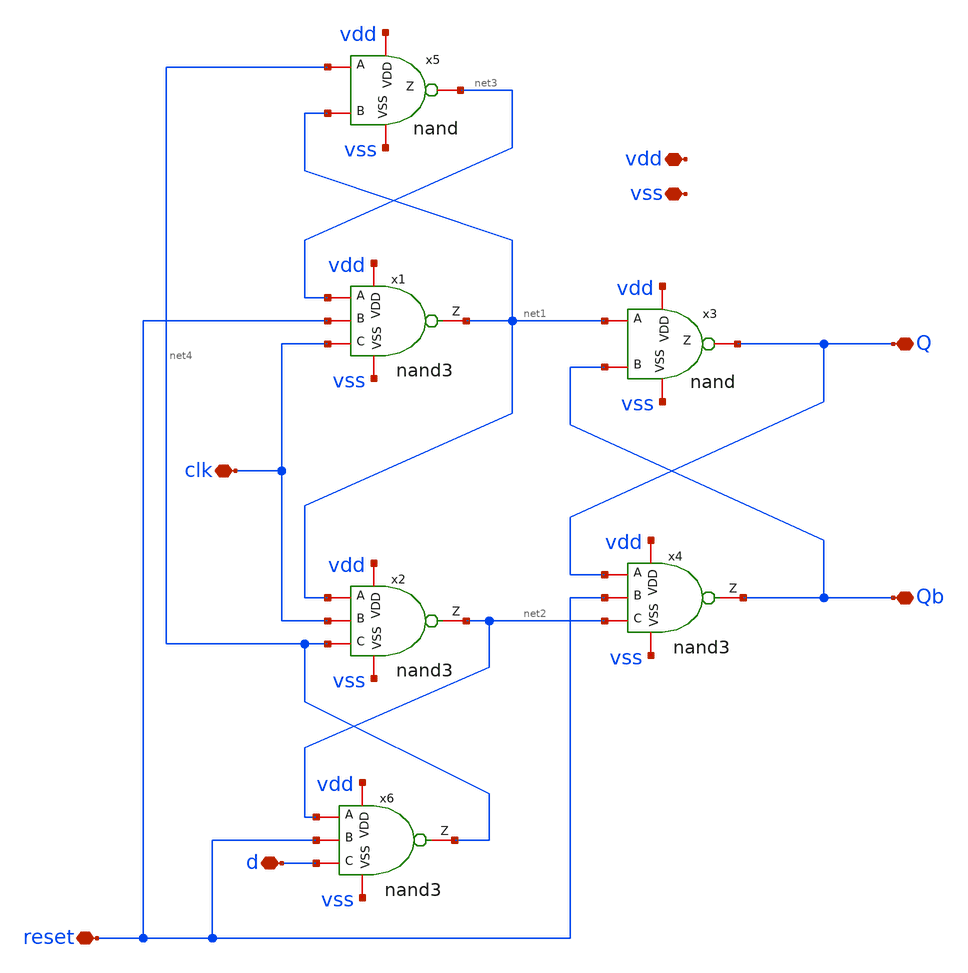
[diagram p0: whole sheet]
** sch_path: designs/libs/adc_singlecycle/dffr.sch
**.subckt dffr vdd vss Q Qb d clk reset
*.iopin vdd
*.iopin vss
*.iopin Q
*.iopin Qb
*.iopin d
*.iopin clk
*.iopin reset
x3 vdd Q net1 Qb vss nand
x2 vdd net2 net1 clk net4 vss nand3
x5 vdd net3 net4 net1 vss nand
x1 vdd net1 net3 reset clk vss nand3
x4 vdd Qb Q reset net2 vss nand3
x6 vdd net4 net2 reset d vss nand3
**.ends
.end
